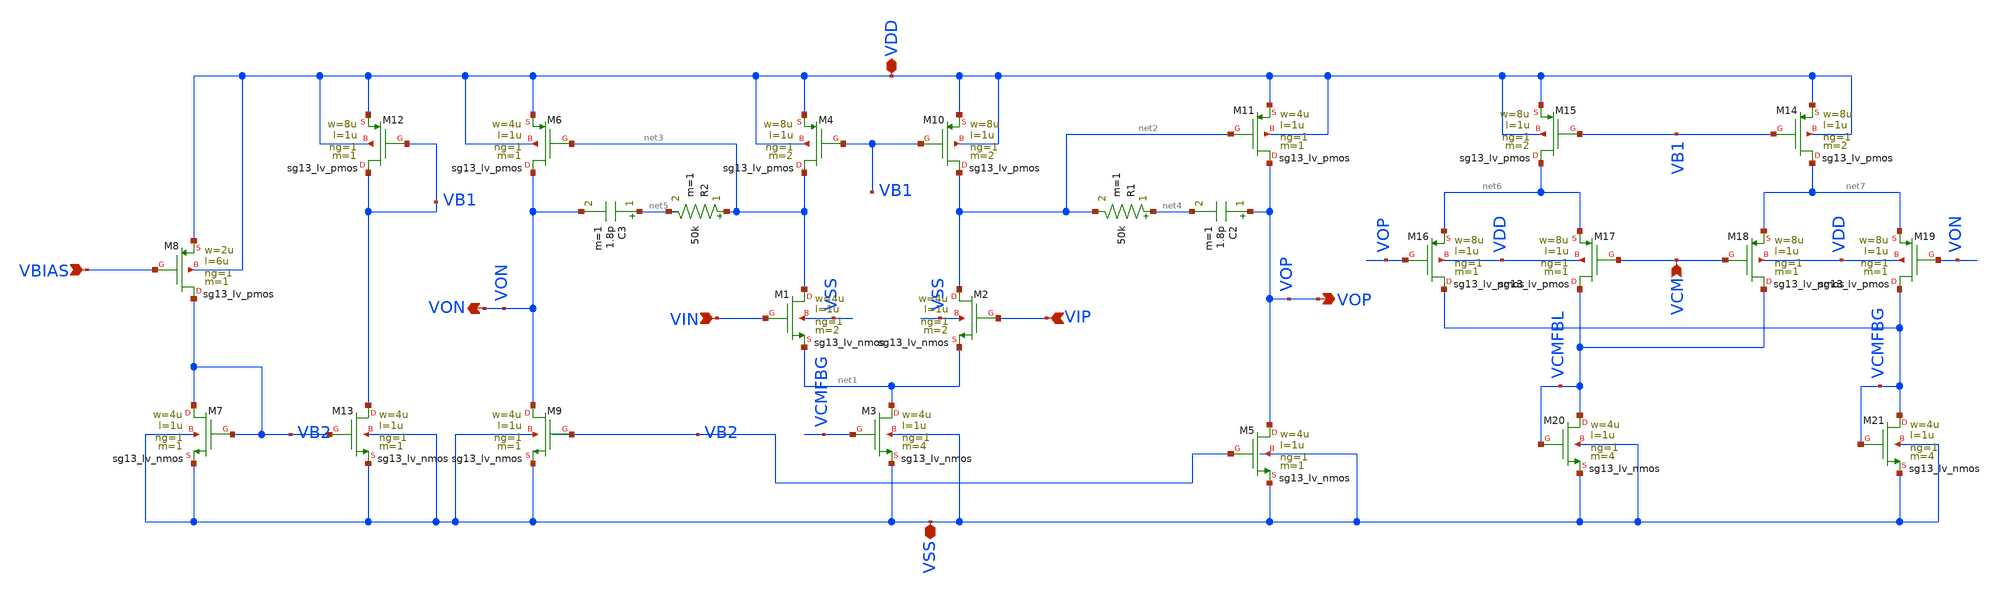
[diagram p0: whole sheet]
** sch_path: BTDay5-Ex/2-stageOpampCMFB.sch
**.subckt 2-stageOpampCMFB VDD VSS VBIAS VON VIN VIP VOP VCM
*.iopin VDD
*.iopin VSS
*.ipin VBIAS
*.opin VON
*.ipin VIN
*.ipin VIP
*.opin VOP
*.ipin VCM
XM1 net3 VIN net1 VSS sg13_lv_nmos w=4u l=1u ng=1 m=2 mm_ok=1
XM2 net2 VIP net1 VSS sg13_lv_nmos w=4u l=1u ng=1 m=2 mm_ok=1
XM3 net1 VCMFBG VSS VSS sg13_lv_nmos w=4u l=1u ng=1 m=4 mm_ok=1
XM4 net3 VB1 VDD VDD sg13_lv_pmos w=8u l=1u ng=1 m=2 mm_ok=1
XM7 VB2 VB2 VSS VSS sg13_lv_nmos w=4u l=1u ng=1 m=1 mm_ok=1
XM8 VB2 VBIAS VDD VDD sg13_lv_pmos w=2u l=6u ng=1 m=1 mm_ok=1
XM10 net2 VB1 VDD VDD sg13_lv_pmos w=8u l=1u ng=1 m=2 mm_ok=1
XM5 VOP VB2 VSS VSS sg13_lv_nmos w=4u l=1u ng=1 m=1 mm_ok=1
XM11 VOP net2 VDD VDD sg13_lv_pmos w=4u l=1u ng=1 m=1 mm_ok=1
C2 VOP net4 1.8p m=1
R1 net4 net2 50k m=1
XM9 VON VB2 VSS VSS sg13_lv_nmos w=4u l=1u ng=1 m=1 mm_ok=1
C3 net5 VON 1.8p m=1
R2 net3 net5 50k m=1
XM12 VB1 VB1 VDD VDD sg13_lv_pmos w=8u l=1u ng=1 m=1 mm_ok=1
XM13 VB1 VB2 VSS VSS sg13_lv_nmos w=4u l=1u ng=1 m=1 mm_ok=1
XM6 VON net3 VDD VDD sg13_lv_pmos w=4u l=1u ng=1 m=1 mm_ok=1
XM14 net7 VB1 VDD VDD sg13_lv_pmos w=8u l=1u ng=1 m=2 mm_ok=1
XM15 net6 VB1 VDD VDD sg13_lv_pmos w=8u l=1u ng=1 m=2 mm_ok=1
XM16 VCMFBG VOP net6 VDD sg13_lv_pmos w=8u l=1u ng=1 m=1 mm_ok=1
XM17 VCMFBL VCM net6 VDD sg13_lv_pmos w=8u l=1u ng=1 m=1 mm_ok=1
XM18 VCMFBL VCM net7 VDD sg13_lv_pmos w=8u l=1u ng=1 m=1 mm_ok=1
XM19 VCMFBG VON net7 VDD sg13_lv_pmos w=8u l=1u ng=1 m=1 mm_ok=1
XM20 VCMFBL VCMFBL VSS VSS sg13_lv_nmos w=4u l=1u ng=1 m=4 mm_ok=1
XM21 VCMFBG VCMFBG VSS VSS sg13_lv_nmos w=4u l=1u ng=1 m=4 mm_ok=1
**.ends
.end
